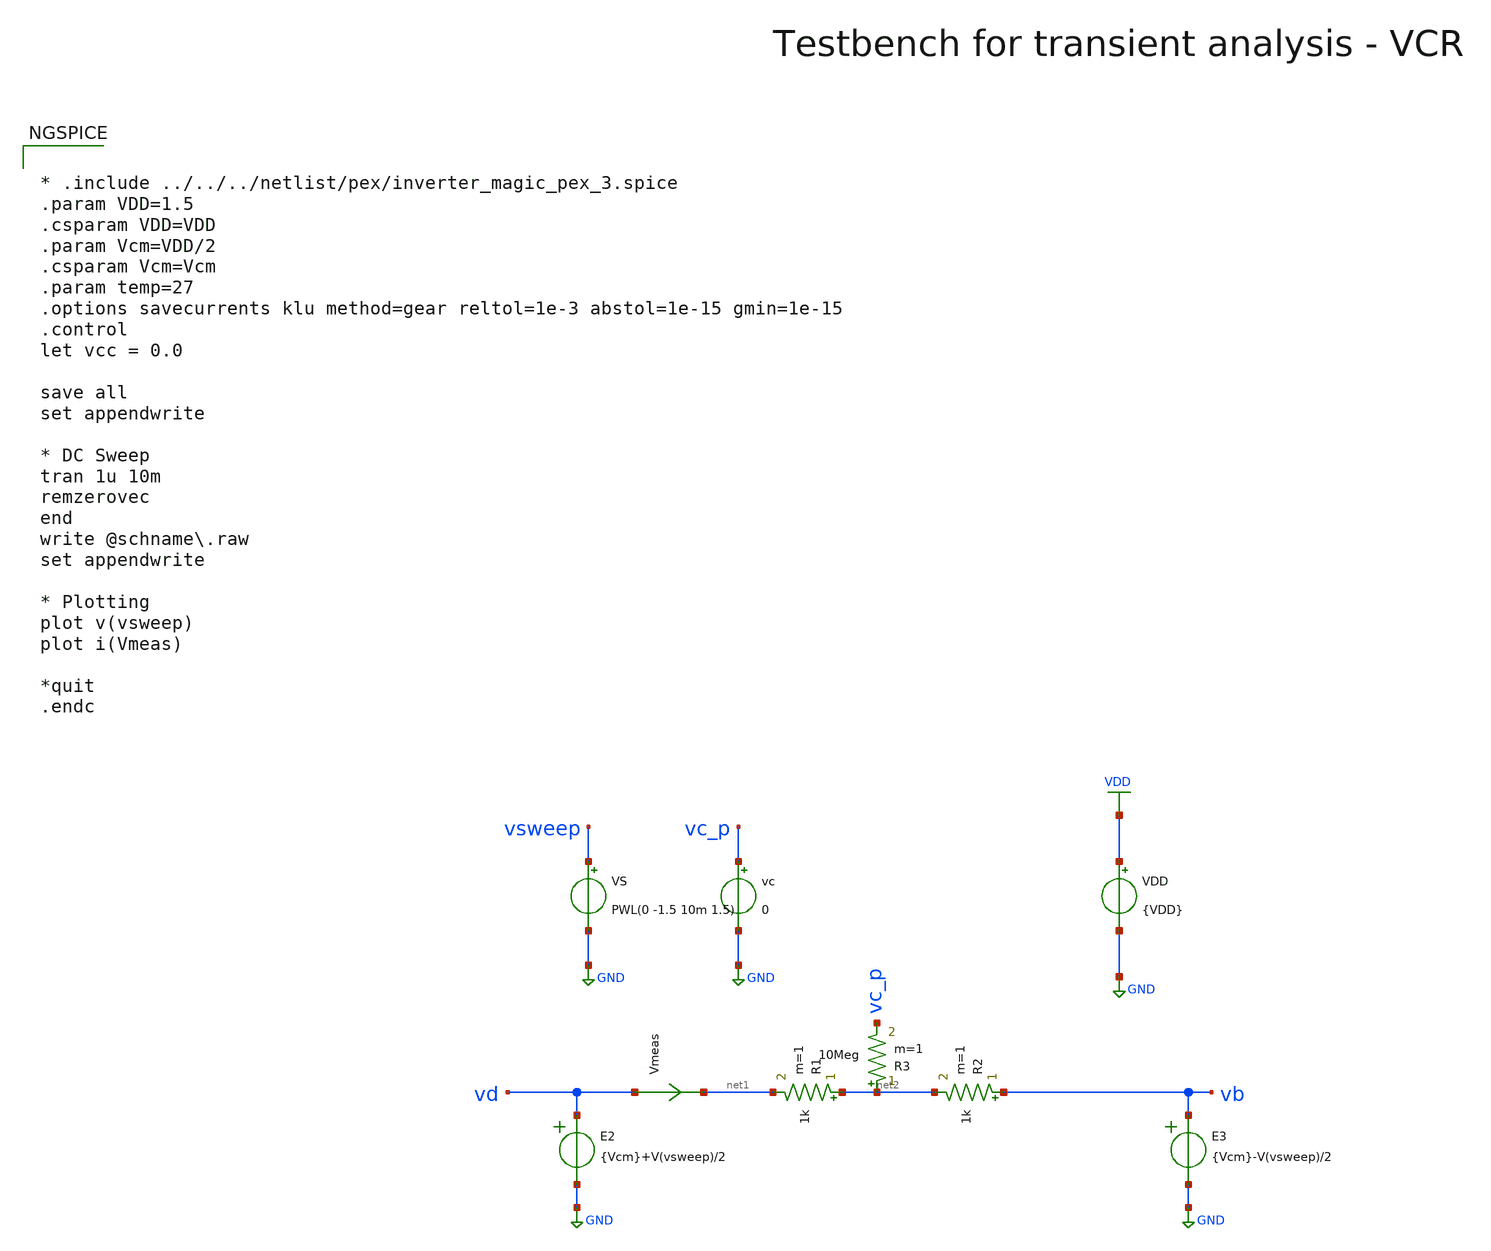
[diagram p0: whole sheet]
** sch_path: macros/heichips26_analog_project/testbenches/xschem/res_tb_tran.sch
**.subckt res_tb_tran
VDD VDD GND {VDD}
R1 net2 net1 1k m=1
VS vsweep GND PWL(0 -1.5 10m 1.5)
Vmeas vd net1 0
.save i(vmeas)
E2 vd GND VOL=' {Vcm}+V(vsweep)/2 '
E3 vb GND VOL=' {Vcm}-V(vsweep)/2 '
vc vc_p GND 0
R2 vb net2 1k m=1
R3 net2 vc_p 10Meg m=1
**** begin user architecture code

.lib cornerMOSlv.lib mos_tt
.lib cornerMOShv.lib mos_tt
.lib cornerRES.lib res_typ
.lib cornerDIO.lib dio_tt



* .include ../../../netlist/pex/inverter_magic_pex_3.spice
.param VDD=1.5
.csparam VDD=VDD
.param Vcm=VDD/2
.csparam Vcm=Vcm
.param temp=27
.options savecurrents klu method=gear reltol=1e-3 abstol=1e-15 gmin=1e-15
.control
let vcc = 0.0

save all
set appendwrite

* DC Sweep
tran 1u 10m
remzerovec
end
write @schname\.raw
set appendwrite

* Plotting
plot v(vsweep)
plot i(Vmeas)

*quit
.endc


**** end user architecture code
**.ends
.GLOBAL GND
.GLOBAL VDD
.end
